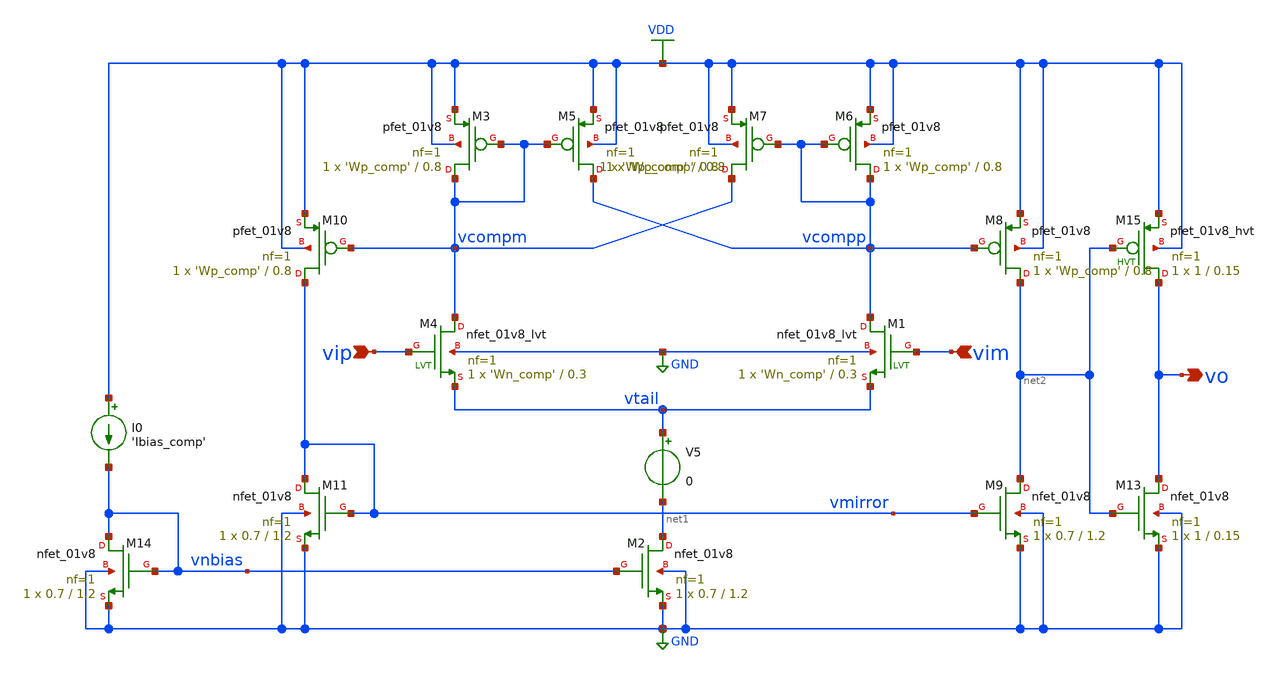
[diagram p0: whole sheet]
** sch_path: designs/comparator.sch
* Copyright 2020 Stefan Frederik Schippers
* Licensed under the Apache License, Version 2.0 (the "License");
* you may not use this file except in compliance with the License.
* You may obtain a copy of the License at
* https://www.apache.org/licenses/LICENSE-2.0
* Unless required by applicable law or agreed to in writing, software
* distributed under the License is distributed on an "AS IS" BASIS,
* WITHOUT WARRANTIES OR CONDITIONS OF ANY KIND, either express or implied.
* See the License for the specific language governing permissions and
* limitations under the License.
**.subckt comparator vip vim vo
*.ipin vip
*.ipin vim
*.opin vo
V5 vtail net1 0
XM6 vcompp vcompp VDD VDD sky130_fd_pr__pfet_01v8 L=0.8 W='Wp_comp' nf=1 ad='int((nf+1)/2) * W/nf * 0.29'
+ as='int((nf+2)/2) * W/nf * 0.29' pd='2*int((nf+1)/2) * (W/nf + 0.29)' ps='2*int((nf+2)/2) * (W/nf + 0.29)'
+ nrd='0.29 / W' nrs='0.29 / W' sa=0 sb=0 sd=0 mult=1 m=1
XM3 vcompm vcompm VDD VDD sky130_fd_pr__pfet_01v8 L=0.8 W='Wp_comp' nf=1 ad='int((nf+1)/2) * W/nf * 0.29'
+ as='int((nf+2)/2) * W/nf * 0.29' pd='2*int((nf+1)/2) * (W/nf + 0.29)' ps='2*int((nf+2)/2) * (W/nf + 0.29)'
+ nrd='0.29 / W' nrs='0.29 / W' sa=0 sb=0 sd=0 mult=1 m=1
XM2 net1 vnbias GND GND sky130_fd_pr__nfet_01v8 L=1.2 W=0.7 nf=1 ad='int((nf+1)/2) * W/nf * 0.29' as='int((nf+2)/2) * W/nf * 0.29'
+ pd='2*int((nf+1)/2) * (W/nf + 0.29)' ps='2*int((nf+2)/2) * (W/nf + 0.29)' nrd='0.29 / W' nrs='0.29 / W'
+ sa=0 sb=0 sd=0 mult=1 m=1
I0 VDD vnbias 'Ibias_comp'
XM14 vnbias vnbias GND GND sky130_fd_pr__nfet_01v8 L=1.2 W=0.7 nf=1 ad='int((nf+1)/2) * W/nf * 0.29'
+ as='int((nf+2)/2) * W/nf * 0.29' pd='2*int((nf+1)/2) * (W/nf + 0.29)' ps='2*int((nf+2)/2) * (W/nf + 0.29)'
+ nrd='0.29 / W' nrs='0.29 / W' sa=0 sb=0 sd=0 mult=1 m=1
XM4 vcompm vip vtail GND sky130_fd_pr__nfet_01v8_lvt L=0.3 W='Wn_comp' nf=1 ad='int((nf+1)/2) * W/nf * 0.29'
+ as='int((nf+2)/2) * W/nf * 0.29' pd='2*int((nf+1)/2) * (W/nf + 0.29)' ps='2*int((nf+2)/2) * (W/nf + 0.29)'
+ nrd='0.29 / W' nrs='0.29 / W' sa=0 sb=0 sd=0 mult=1 m=1
XM1 vcompp vim vtail GND sky130_fd_pr__nfet_01v8_lvt L=0.3 W='Wn_comp' nf=1 ad='int((nf+1)/2) * W/nf * 0.29'
+ as='int((nf+2)/2) * W/nf * 0.29' pd='2*int((nf+1)/2) * (W/nf + 0.29)' ps='2*int((nf+2)/2) * (W/nf + 0.29)'
+ nrd='0.29 / W' nrs='0.29 / W' sa=0 sb=0 sd=0 mult=1 m=1
XM5 vcompp vcompm VDD VDD sky130_fd_pr__pfet_01v8 L=0.8 W='Wp_comp' nf=1 ad='int((nf+1)/2) * W/nf * 0.29'
+ as='int((nf+2)/2) * W/nf * 0.29' pd='2*int((nf+1)/2) * (W/nf + 0.29)' ps='2*int((nf+2)/2) * (W/nf + 0.29)'
+ nrd='0.29 / W' nrs='0.29 / W' sa=0 sb=0 sd=0 mult=1 m=1
XM7 vcompm vcompp VDD VDD sky130_fd_pr__pfet_01v8 L=0.8 W='Wp_comp' nf=1 ad='int((nf+1)/2) * W/nf * 0.29'
+ as='int((nf+2)/2) * W/nf * 0.29' pd='2*int((nf+1)/2) * (W/nf + 0.29)' ps='2*int((nf+2)/2) * (W/nf + 0.29)'
+ nrd='0.29 / W' nrs='0.29 / W' sa=0 sb=0 sd=0 mult=1 m=1
XM8 net2 vcompp VDD VDD sky130_fd_pr__pfet_01v8 L=0.8 W='Wp_comp' nf=1 ad='int((nf+1)/2) * W/nf * 0.29'
+ as='int((nf+2)/2) * W/nf * 0.29' pd='2*int((nf+1)/2) * (W/nf + 0.29)' ps='2*int((nf+2)/2) * (W/nf + 0.29)'
+ nrd='0.29 / W' nrs='0.29 / W' sa=0 sb=0 sd=0 mult=1 m=1
XM9 net2 vmirror GND GND sky130_fd_pr__nfet_01v8 L=1.2 W=0.7 nf=1 ad='int((nf+1)/2) * W/nf * 0.29' as='int((nf+2)/2) * W/nf * 0.29'
+ pd='2*int((nf+1)/2) * (W/nf + 0.29)' ps='2*int((nf+2)/2) * (W/nf + 0.29)' nrd='0.29 / W' nrs='0.29 / W'
+ sa=0 sb=0 sd=0 mult=1 m=1
XM10 vmirror vcompm VDD VDD sky130_fd_pr__pfet_01v8 L=0.8 W='Wp_comp' nf=1 ad='int((nf+1)/2) * W/nf * 0.29'
+ as='int((nf+2)/2) * W/nf * 0.29' pd='2*int((nf+1)/2) * (W/nf + 0.29)' ps='2*int((nf+2)/2) * (W/nf + 0.29)'
+ nrd='0.29 / W' nrs='0.29 / W' sa=0 sb=0 sd=0 mult=1 m=1
XM11 vmirror vmirror GND GND sky130_fd_pr__nfet_01v8 L=1.2 W=0.7 nf=1 ad='int((nf+1)/2) * W/nf * 0.29'
+ as='int((nf+2)/2) * W/nf * 0.29' pd='2*int((nf+1)/2) * (W/nf + 0.29)' ps='2*int((nf+2)/2) * (W/nf + 0.29)'
+ nrd='0.29 / W' nrs='0.29 / W' sa=0 sb=0 sd=0 mult=1 m=1
XM13 vo net2 GND GND sky130_fd_pr__nfet_01v8 L=0.15 W=1 nf=1 ad='int((nf+1)/2) * W/nf * 0.29' as='int((nf+2)/2) * W/nf * 0.29'
+ pd='2*int((nf+1)/2) * (W/nf + 0.29)' ps='2*int((nf+2)/2) * (W/nf + 0.29)' nrd='0.29 / W' nrs='0.29 / W'
+ sa=0 sb=0 sd=0 mult=1 m=1
XM15 vo net2 VDD VDD sky130_fd_pr__pfet_01v8_hvt L=0.15 W=1 nf=1 ad='int((nf+1)/2) * W/nf * 0.29' as='int((nf+2)/2) * W/nf * 0.29'
+ pd='2*int((nf+1)/2) * (W/nf + 0.29)' ps='2*int((nf+2)/2) * (W/nf + 0.29)' nrd='0.29 / W' nrs='0.29 / W'
+ sa=0 sb=0 sd=0 mult=1 m=1
**** begin user architecture code

.include $::SKYWATER_MODELS/cells/nfet_01v8/sky130_fd_pr__nfet_01v8__tt.corner.spice
.include $::SKYWATER_MODELS/cells/nfet_01v8_lvt/sky130_fd_pr__nfet_01v8_lvt__tt.corner.spice
.include $::SKYWATER_MODELS/cells/pfet_01v8/sky130_fd_pr__pfet_01v8__tt.corner.spice
.include $::SKYWATER_MODELS/cells/nfet_03v3_nvt/sky130_fd_pr__nfet_03v3_nvt__tt.corner.spice
.include $::SKYWATER_MODELS/cells/nfet_05v0_nvt/sky130_fd_pr__nfet_05v0_nvt__tt.corner.spice
.include $::SKYWATER_MODELS/cells/esd_nfet_01v8/sky130_fd_pr__esd_nfet_01v8__tt.corner.spice
.include $::SKYWATER_MODELS/cells/pfet_01v8_lvt/sky130_fd_pr__pfet_01v8_lvt__tt.corner.spice
.include $::SKYWATER_MODELS/cells/pfet_01v8_hvt/sky130_fd_pr__pfet_01v8_hvt__tt.corner.spice
.include $::SKYWATER_MODELS/cells/esd_pfet_g5v0d10v5/sky130_fd_pr__esd_pfet_g5v0d10v5__tt.corner.spice
.include $::SKYWATER_MODELS/cells/pfet_g5v0d10v5/sky130_fd_pr__pfet_g5v0d10v5__tt.corner.spice
.include $::SKYWATER_MODELS/cells/pfet_g5v0d16v0/sky130_fd_pr__pfet_g5v0d16v0__tt.corner.spice
.include $::SKYWATER_MODELS/cells/nfet_g5v0d10v5/sky130_fd_pr__nfet_g5v0d10v5__tt.corner.spice
.include $::SKYWATER_MODELS/cells/nfet_g5v0d16v0/sky130_fd_pr__nfet_g5v0d16v0__tt_discrete.corner.spice
.include $::SKYWATER_MODELS/cells/esd_nfet_g5v0d10v5/sky130_fd_pr__esd_nfet_g5v0d10v5__tt.corner.spice
.include $::SKYWATER_MODELS/models/corners/tt/nonfet.spice
* Mismatch parameters
.include $::SKYWATER_MODELS/cells/nfet_01v8/sky130_fd_pr__nfet_01v8__mismatch.corner.spice
.include $::SKYWATER_MODELS/cells/pfet_01v8/sky130_fd_pr__pfet_01v8__mismatch.corner.spice
.include $::SKYWATER_MODELS/cells/nfet_01v8_lvt/sky130_fd_pr__nfet_01v8_lvt__mismatch.corner.spice
.include $::SKYWATER_MODELS/cells/pfet_01v8_lvt/sky130_fd_pr__pfet_01v8_lvt__mismatch.corner.spice
.include $::SKYWATER_MODELS/cells/pfet_01v8_hvt/sky130_fd_pr__pfet_01v8_hvt__mismatch.corner.spice
.include $::SKYWATER_MODELS/cells/nfet_g5v0d10v5/sky130_fd_pr__nfet_g5v0d10v5__mismatch.corner.spice
.include $::SKYWATER_MODELS/cells/pfet_g5v0d10v5/sky130_fd_pr__pfet_g5v0d10v5__mismatch.corner.spice
.include $::SKYWATER_MODELS/cells/nfet_05v0_nvt/sky130_fd_pr__nfet_05v0_nvt__mismatch.corner.spice
.include $::SKYWATER_MODELS/cells/nfet_03v3_nvt/sky130_fd_pr__nfet_03v3_nvt__mismatch.corner.spice
* Resistor$::SKYWATER_MODELS/Capacitor
.include $::SKYWATER_MODELS/models/r+c/res_typical__cap_typical.spice
.include $::SKYWATER_MODELS/models/r+c/res_typical__cap_typical__lin.spice
* Special cells
.include $::SKYWATER_MODELS/models/corners/tt/specialized_cells.spice
* All models
.include $::SKYWATER_MODELS/models/all.spice
* Corner
.include $::SKYWATER_MODELS/models/corners/tt/rf.spice

**** end user architecture code
**.ends
.GLOBAL VDD
.GLOBAL GND
**** begin user architecture code

.include comparator_commands.spice

**** end user architecture code
.end
